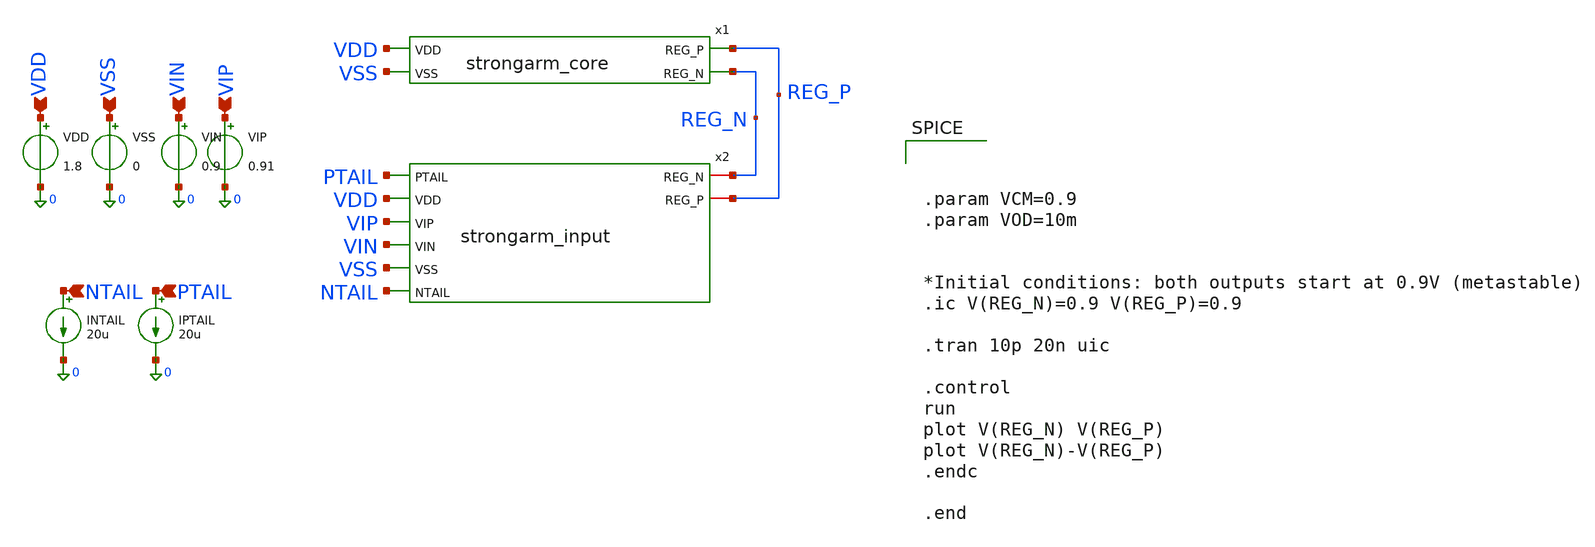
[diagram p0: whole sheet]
** sch_path: tb_input_core.sch
**.subckt tb_input_core VDD VSS VIN VIP NTAIL PTAIL
*.ipin VDD
*.ipin VSS
*.ipin VIN
*.ipin VIP
*.ipin NTAIL
*.ipin PTAIL
x1 VDD REG_P REG_N VSS strongarm_core
x2 PTAIL VDD REG_N REG_P VIP VIN VSS NTAIL strongarm_input
VDD VDD 0 1.8
VSS VSS 0 0
VIN VIN 0 0.9
VIP VIP 0 0.91
INTAIL NTAIL 0 20u
IPTAIL PTAIL 0 20u
**** begin user architecture code

** opencircuitdesign pdks install
.lib $::SKYWATER_MODELS/sky130.lib.spice tt




.param VCM=0.9
.param VOD=10m


*Initial conditions: both outputs start at 0.9V (metastable)
.ic V(REG_N)=0.9 V(REG_P)=0.9

.tran 10p 20n uic

.control
run
plot V(REG_N) V(REG_P)
plot V(REG_N)-V(REG_P)
.endc

.end

**** end user architecture code
**.ends

* expanding   symbol:  /home/master/Documents/6_bit_Flash_ADC/strongarm_core.sym # of pins=4
** sym_path: strongarm_core.sym
** sch_path: strongarm_core.sch
.subckt strongarm_core VDD REG_P REG_N VSS
*.ipin VDD
*.ipin VSS
*.opin REG_P
*.opin REG_N
XM8 REG_P REG_N VDD VDD sky130_fd_pr__pfet_01v8 L=0.15 W=12 nf=1 ad='int((1 + 1)/2) * 12 / 1 * 0.29'
+ as='int((1 + 2)/2) * 12 / 1 * 0.29' pd='2*int((1 + 1)/2) * (12 / 1 + 0.29)' ps='2*int((1 + 2)/2) * (12 / 1 + 0.29)'
+ nrd='0.29 / 12 ' nrs='0.29 / 12 ' sa=0 sb=0 sd=0 mult=1 m=1
XM6 REG_P REG_N VSS VSS sky130_fd_pr__nfet_01v8 L=0.15 W=6 nf=1 ad='int((1 + 1)/2) * 6 / 1 * 0.29' as='int((1 + 2)/2) * 6 / 1 * 0.29'
+ pd='2*int((1 + 1)/2) * (6 / 1 + 0.29)' ps='2*int((1 + 2)/2) * (6 / 1 + 0.29)' nrd='0.29 / 6 ' nrs='0.29 / 6 '
+ sa=0 sb=0 sd=0 mult=1 m=1
XM5 REG_N REG_P VSS VSS sky130_fd_pr__nfet_01v8 L=0.15 W=6 nf=1 ad='int((1 + 1)/2) * 6 / 1 * 0.29' as='int((1 + 2)/2) * 6 / 1 * 0.29'
+ pd='2*int((1 + 1)/2) * (6 / 1 + 0.29)' ps='2*int((1 + 2)/2) * (6 / 1 + 0.29)' nrd='0.29 / 6 ' nrs='0.29 / 6 '
+ sa=0 sb=0 sd=0 mult=1 m=1
XM7 REG_N REG_P VDD VDD sky130_fd_pr__pfet_01v8 L=0.15 W=12 nf=1 ad='int((1 + 1)/2) * 12 / 1 * 0.29'
+ as='int((1 + 2)/2) * 12 / 1 * 0.29' pd='2*int((1 + 1)/2) * (12 / 1 + 0.29)' ps='2*int((1 + 2)/2) * (12 / 1 + 0.29)'
+ nrd='0.29 / 12 ' nrs='0.29 / 12 ' sa=0 sb=0 sd=0 mult=1 m=1
.ends


* expanding   symbol:  /home/master/Documents/6_bit_Flash_ADC/strongarm_input.sym # of pins=8
** sym_path: strongarm_input.sym
** sch_path: strongarm_input.sch
.subckt strongarm_input PTAIL VDD REG_N REG_P VIP VIN VSS NTAIL
*.ipin PTAIL
*.ipin NTAIL
*.iopin REG_P
*.iopin REG_N
*.ipin VSS
*.ipin VDD
*.ipin VIP
*.ipin VIN
XM1 REG_N VIN NTAIL VSS sky130_fd_pr__nfet_01v8 L=0.15 W=12 nf=2 ad='int((2 + 1)/2) * 12 / 2 * 0.29'
+ as='int((2 + 2)/2) * 12 / 2 * 0.29' pd='2*int((2 + 1)/2) * (12 / 2 + 0.29)' ps='2*int((2 + 2)/2) * (12 / 2 + 0.29)'
+ nrd='0.29 / 12 ' nrs='0.29 / 12 ' sa=0 sb=0 sd=0 mult=1 m=1
XM2 REG_P VIP NTAIL VSS sky130_fd_pr__nfet_01v8 L=0.15 W=12 nf=2 ad='int((2 + 1)/2) * 12 / 2 * 0.29'
+ as='int((2 + 2)/2) * 12 / 2 * 0.29' pd='2*int((2 + 1)/2) * (12 / 2 + 0.29)' ps='2*int((2 + 2)/2) * (12 / 2 + 0.29)'
+ nrd='0.29 / 12 ' nrs='0.29 / 12 ' sa=0 sb=0 sd=0 mult=1 m=1
XM3 REG_N VIN PTAIL VDD sky130_fd_pr__pfet_01v8 L=0.15 W=24 nf=2 ad='int((2 + 1)/2) * 24 / 2 * 0.29'
+ as='int((2 + 2)/2) * 24 / 2 * 0.29' pd='2*int((2 + 1)/2) * (24 / 2 + 0.29)' ps='2*int((2 + 2)/2) * (24 / 2 + 0.29)'
+ nrd='0.29 / 24 ' nrs='0.29 / 24 ' sa=0 sb=0 sd=0 mult=1 m=1
XM4 REG_P VIP PTAIL VDD sky130_fd_pr__pfet_01v8 L=0.15 W=24 nf=2 ad='int((2 + 1)/2) * 24 / 2 * 0.29'
+ as='int((2 + 2)/2) * 24 / 2 * 0.29' pd='2*int((2 + 1)/2) * (24 / 2 + 0.29)' ps='2*int((2 + 2)/2) * (24 / 2 + 0.29)'
+ nrd='0.29 / 24 ' nrs='0.29 / 24 ' sa=0 sb=0 sd=0 mult=1 m=1
.ends

.end
